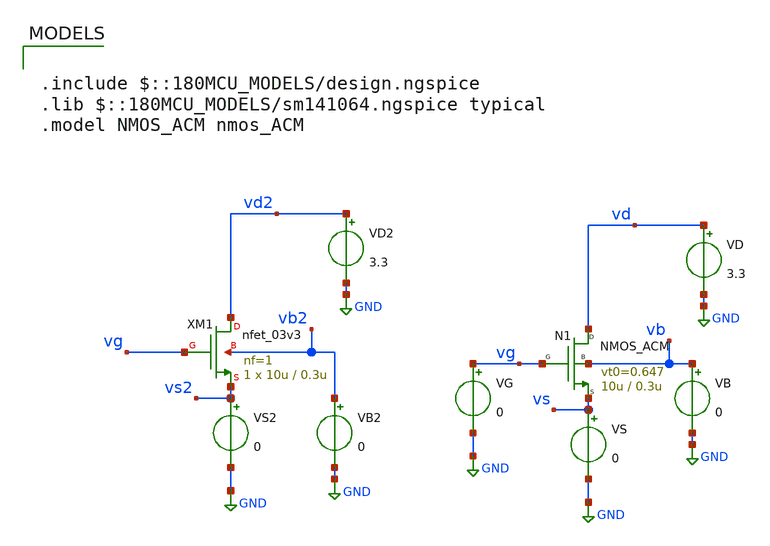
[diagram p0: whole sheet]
** sch_path: legacy/Examples/GF180MCU/xschem/Extraction/TB_nmos_acm.sch
**.subckt TB_nmos_acm
VG vg GND 0
VD vd GND 3.3
VB vb GND 0
VS vs GND 0
VD2 vd2 GND 3.3
VB2 vb2 GND 0
VS2 vs2 GND 0
XM1 vd2 vg vs2 vb2 nfet_03v3 L=0.3u W=10u nf=1 ad='int((nf+1)/2) * W/nf * 0.18u' as='int((nf+2)/2) * W/nf * 0.18u'
+ pd='2*int((nf+1)/2) * (W/nf + 0.18u)' ps='2*int((nf+2)/2) * (W/nf + 0.18u)' nrd='0.18u / W' nrs='0.18u / W'
+ sa=0 sb=0 sd=0 m=1
N1 vd vg vs vb NMOS_ACM w=10u l=0.3u n=1.37 is=2.15u vt0=0.647 sigma=26m zeta=24m
**** begin user architecture code

.include $::180MCU_MODELS/design.ngspice
.lib $::180MCU_MODELS/sm141064.ngspice typical
.model NMOS_ACM nmos_ACM



.control
pre_osdi ./NMOS_ACM_2V0.osdi
save all

dc VG 0.1 3.3 5m


*gm for ACM
let gm_id = deriv(ln(i(Vs)))

*gm for GF180
let gm_id_gf = deriv(ln(i(Vs2)))

save gm_id gm_id_gf
write TB_nmos_acm.raw

.endc


**** end user architecture code
**.ends
.GLOBAL GND
.end
